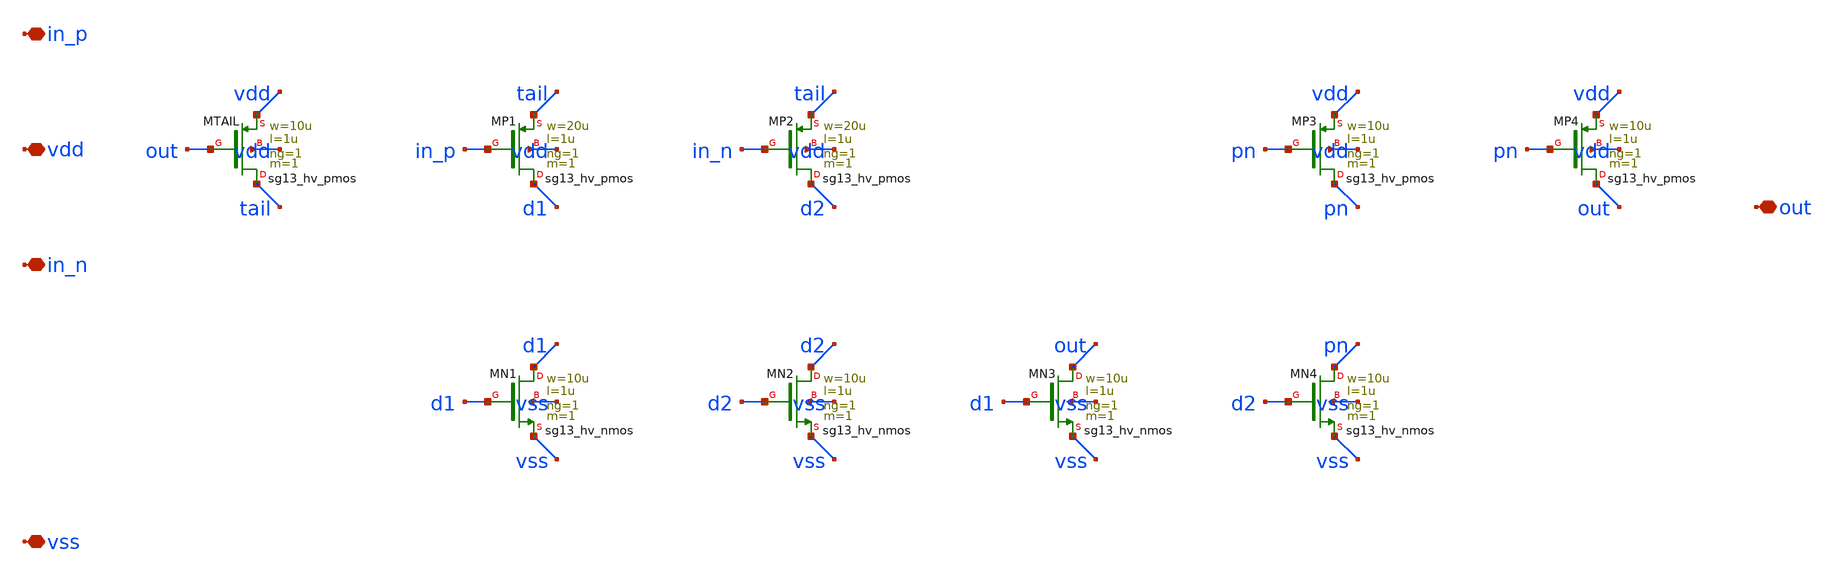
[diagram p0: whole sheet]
** sch_path: designs/g1-guardian/blocks/g1_bgr/source/2AMLogic-sg13g2-bandgap/bandgap_amp.sch
**.subckt bandgap_amp vdd vss in_p in_n out
*.iopin vdd
*.iopin vss
*.iopin in_p
*.iopin in_n
*.iopin out
XMTAIL tail out vdd vdd sg13_hv_pmos w=10u l=1u ng=1 m=1 mm_ok=1
XMP1 d1 in_p tail vdd sg13_hv_pmos w=20u l=1u ng=1 m=1 mm_ok=1
XMP2 d2 in_n tail vdd sg13_hv_pmos w=20u l=1u ng=1 m=1 mm_ok=1
XMP3 pn pn vdd vdd sg13_hv_pmos w=10u l=1u ng=1 m=1 mm_ok=1
XMP4 out pn vdd vdd sg13_hv_pmos w=10u l=1u ng=1 m=1 mm_ok=1
XMN1 d1 d1 vss vss sg13_hv_nmos w=10u l=1u ng=1 m=1 mm_ok=1
XMN2 d2 d2 vss vss sg13_hv_nmos w=10u l=1u ng=1 m=1 mm_ok=1
XMN3 out d1 vss vss sg13_hv_nmos w=10u l=1u ng=1 m=1 mm_ok=1
XMN4 pn d2 vss vss sg13_hv_nmos w=10u l=1u ng=1 m=1 mm_ok=1
**.ends
.end
